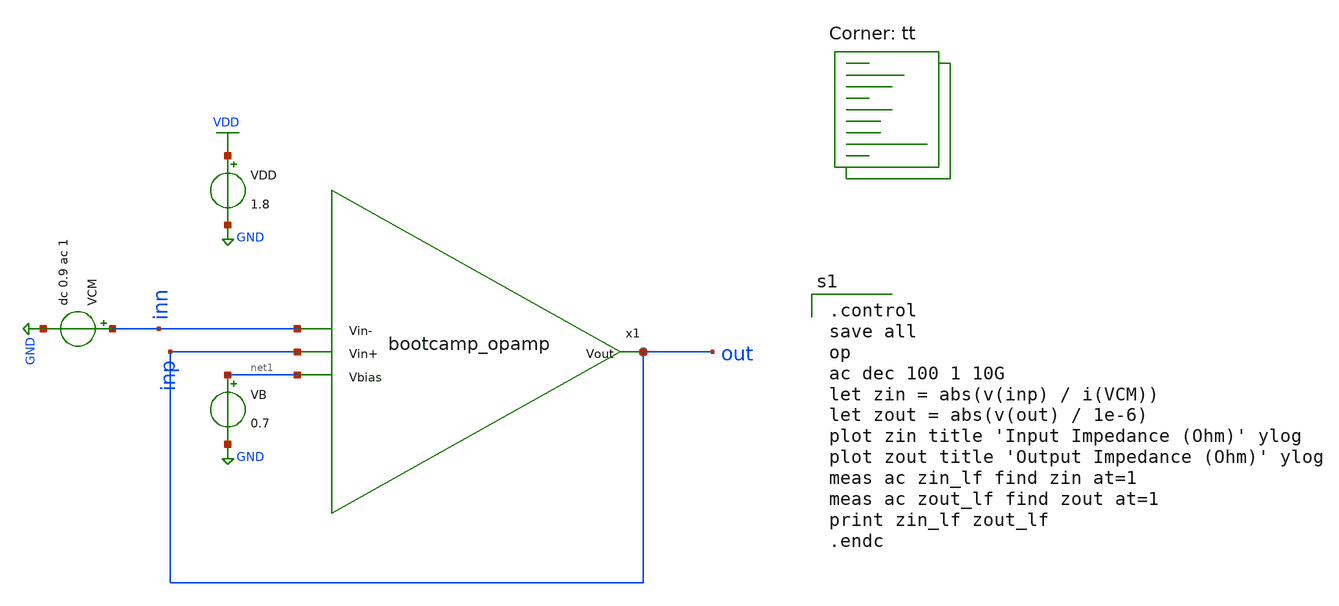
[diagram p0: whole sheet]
** sch_path: analog/build/schematic/untitled.sch
**.subckt untitled
x1 out inn out net1 bootcamp_opamp
VDD VDD GND 1.8
VB net1 GND 0.7
VCM inn GND dc 0.9 ac 1
**** begin user architecture code

.control
save all
op
ac dec 100 1 10G
let zin = abs(v(inp) / i(VCM))
let zout = abs(v(out) / 1e-6)
plot zin title 'Input Impedance (Ohm)' ylog
plot zout title 'Output Impedance (Ohm)' ylog
meas ac zin_lf find zin at=1
meas ac zout_lf find zout at=1
print zin_lf zout_lf
.endc

.lib $::SKYWATER_MODELS/sky130.lib.spice tt
**** end user architecture code
**.ends
.GLOBAL GND
.GLOBAL VDD
.end
